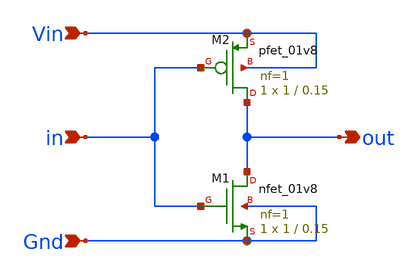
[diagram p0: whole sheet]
** sch_path: Inverter-Ringoscillator/inverter.sch
**.subckt inverter in Vin Gnd out
*.ipin in
*.ipin Vin
*.ipin Gnd
*.opin out
XM1 out in Gnd Gnd sky130_fd_pr__nfet_01v8 L=0.15 W=1 nf=1 ad='int((nf+1)/2) * W/nf * 0.29' as='int((nf+2)/2) * W/nf * 0.29'
+ pd='2*int((nf+1)/2) * (W/nf + 0.29)' ps='2*int((nf+2)/2) * (W/nf + 0.29)' nrd='0.29 / W' nrs='0.29 / W'
+ sa=0 sb=0 sd=0 mult=1 m=1
XM2 out in Vin Vin sky130_fd_pr__pfet_01v8 L=0.15 W=1 nf=1 ad='int((nf+1)/2) * W/nf * 0.29' as='int((nf+2)/2) * W/nf * 0.29'
+ pd='2*int((nf+1)/2) * (W/nf + 0.29)' ps='2*int((nf+2)/2) * (W/nf + 0.29)' nrd='0.29 / W' nrs='0.29 / W'
+ sa=0 sb=0 sd=0 mult=1 m=1
**.ends
.end
